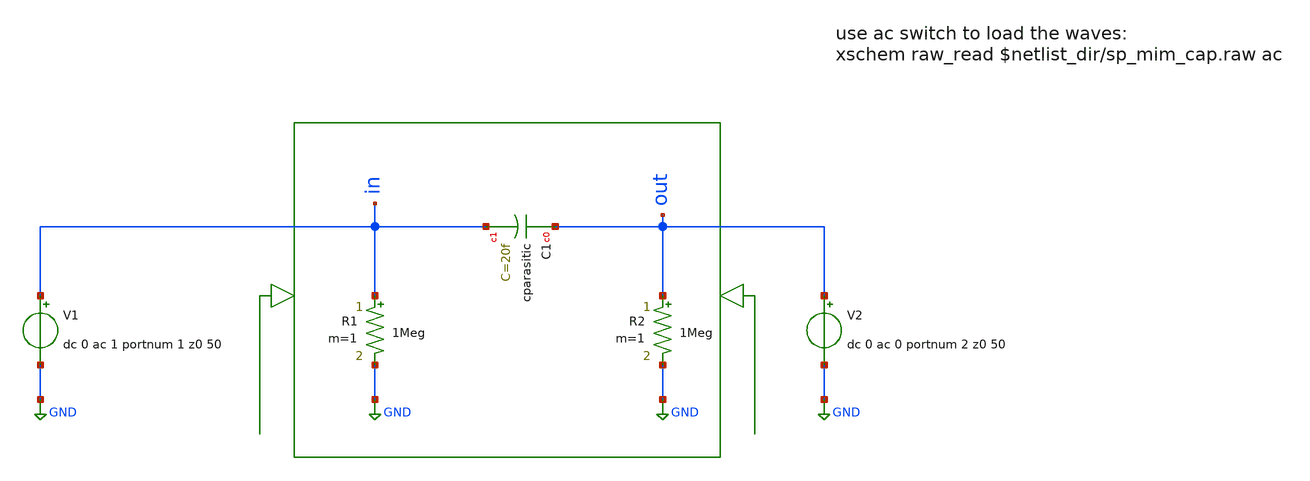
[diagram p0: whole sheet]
** sch_path: ihp-sg13g2/xschem_libs/sg13g2_tests_ase/sp_parasitic_cap/schematic/sp_parasitic_cap.sch
* Copyright 2021 Stefan Frederik Schippers
* Licensed under the Apache License, Version 2.0 (the "License");
* you may not use this file except in compliance with the License.
* You may obtain a copy of the License at
* https://www.apache.org/licenses/LICENSE-2.0
* Unless required by applicable law or agreed to in writing, software
* distributed under the License is distributed on an "AS IS" BASIS,
* WITHOUT WARRANTIES OR CONDITIONS OF ANY KIND, either express or implied.
* See the License for the specific language governing permissions and
* limitations under the License.
* Copyright 2023 IHP PDK Authors
**.subckt sp_parasitic_cap
R1 in GND 1Meg m=1
V1 in GND dc 0 ac 1 portnum 1 z0 50
R2 out GND 1Meg m=1
V2 out GND dc 0 ac 0 portnum 2 z0 50
XC1 out in cparasitic C=20f
**.ends
.GLOBAL GND
.end
